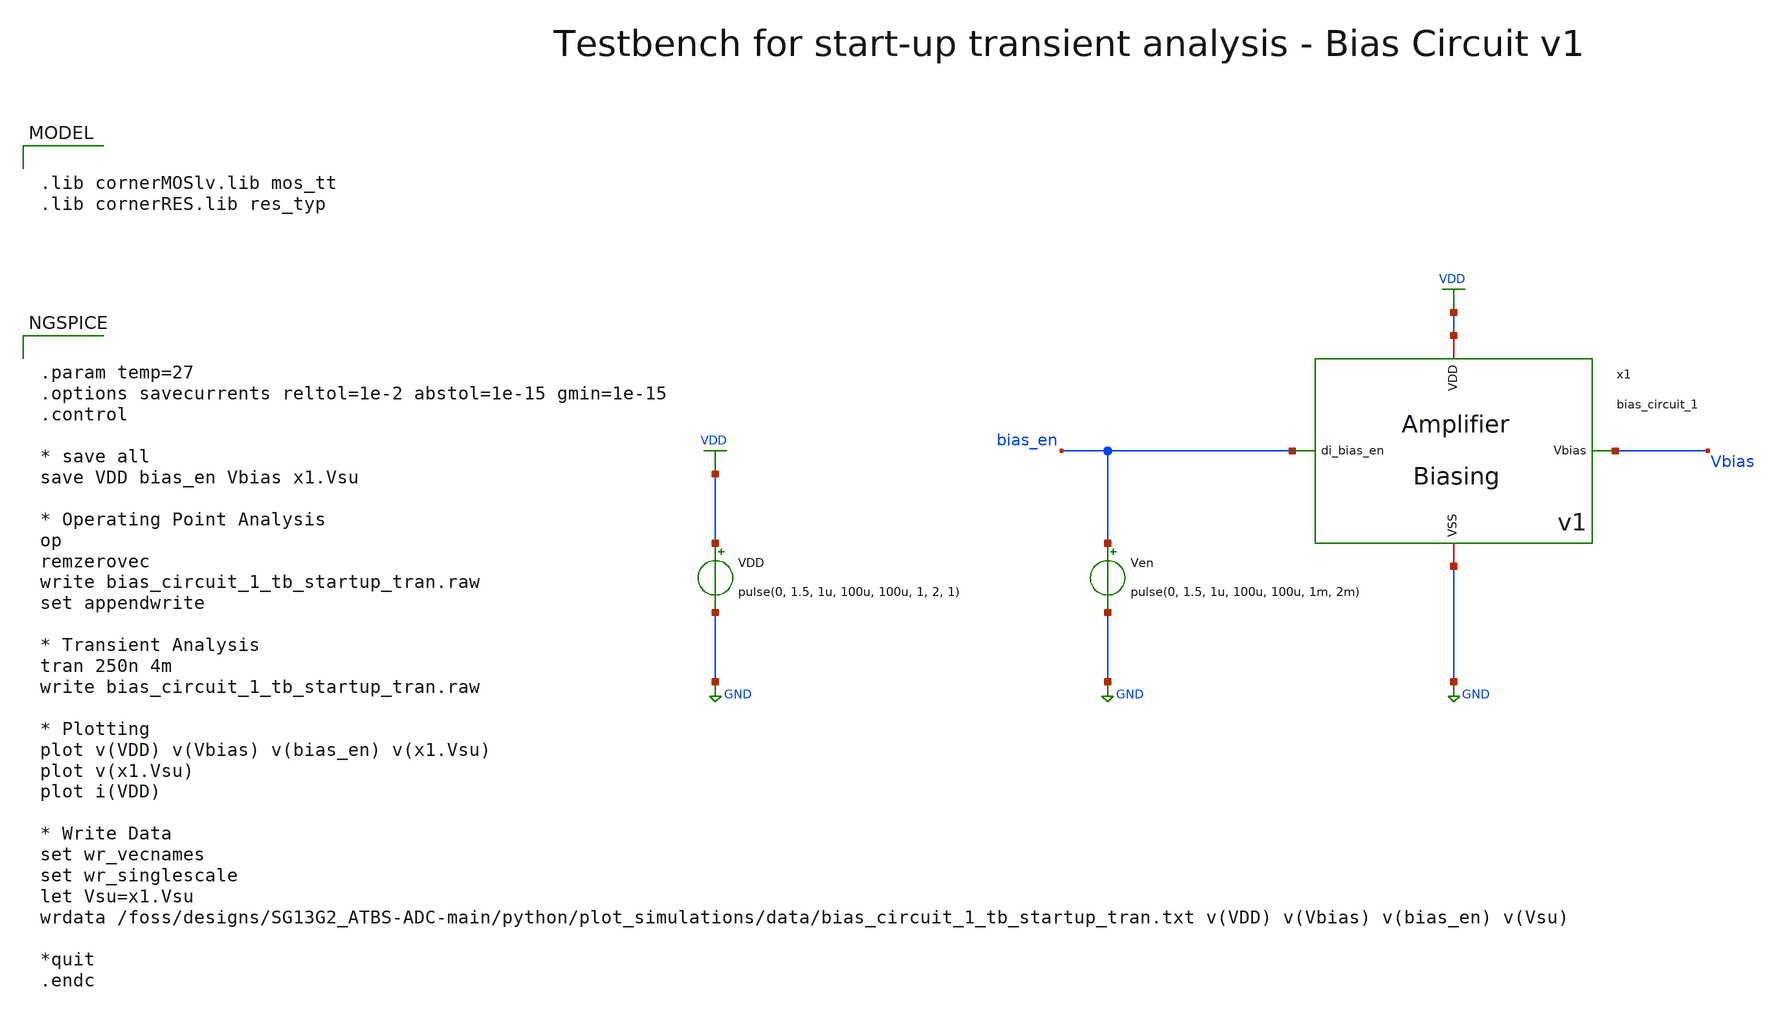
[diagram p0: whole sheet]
** sch_path: SG13G2_ATBS-ADC-main/xschem/bio_amplifier/amplifier_core/bias_circuit/bias_circuit_1/testbenches/bias_circuit_1_tb_startup_tran.sch
**.subckt bias_circuit_1_tb_startup_tran
x1 bias_en Vbias VDD GND bias_circuit_1
Ven bias_en GND pulse(0, 1.5, 1u, 100u, 100u, 1m, 2m)
VDD VDD GND pulse(0, 1.5, 1u, 100u, 100u, 1, 2, 1)
**** begin user architecture code

.lib cornerMOSlv.lib mos_tt
.lib cornerRES.lib res_typ



.param temp=27
.options savecurrents reltol=1e-2 abstol=1e-15 gmin=1e-15
.control

* save all
save VDD bias_en Vbias x1.Vsu

* Operating Point Analysis
op
remzerovec
write bias_circuit_1_tb_startup_tran.raw
set appendwrite

* Transient Analysis
tran 250n 4m
write bias_circuit_1_tb_startup_tran.raw

* Plotting
plot v(VDD) v(Vbias) v(bias_en) v(x1.Vsu)
plot v(x1.Vsu)
plot i(VDD)

* Write Data
set wr_vecnames
set wr_singlescale
let Vsu=x1.Vsu
wrdata
+ /foss/designs/SG13G2_ATBS-ADC-main/python/plot_simulations/data/bias_circuit_1_tb_startup_tran.txt v(VDD) v(Vbias) v(bias_en) v(Vsu)

*quit
.endc

**** end user architecture code
**.ends
.GLOBAL GND
.GLOBAL VDD
.end
